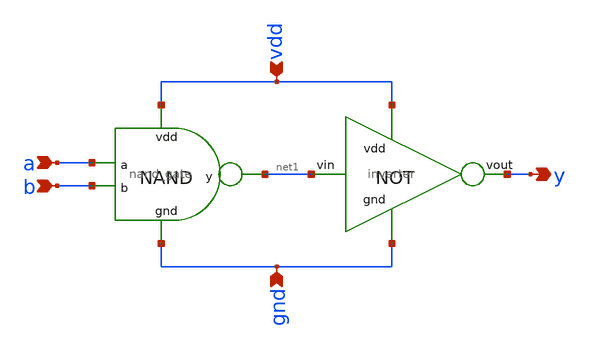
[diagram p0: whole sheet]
** sch_path: sram/and_gate.sch
**.subckt and_gate a b vdd gnd y
*.ipin a
*.ipin b
*.ipin vdd
*.ipin gnd
*.opin y
x2 vdd net1 y gnd inverter
x1 vdd a b gnd net1 nand_gate
**.ends

* expanding   symbol:  inverter.sym # of pins=4
** sym_path: sram/inverter.sym
** sch_path: sram/inverter.sch
.subckt inverter vdd vin vout gnd
*.ipin vin
*.ipin vdd
*.ipin gnd
*.opin vout
XM1 vout vin gnd gnd sky130_fd_pr__nfet_01v8 L=0.15 W=1 nf=1 ad='int((nf+1)/2) * W/nf * 0.29' as='int((nf+2)/2) * W/nf * 0.29'
+ pd='2*int((nf+1)/2) * (W/nf + 0.29)' ps='2*int((nf+2)/2) * (W/nf + 0.29)' nrd='0.29 / W' nrs='0.29 / W'
+ sa=0 sb=0 sd=0 mult=1 m=1
XM2 vout vin vdd vdd sky130_fd_pr__pfet_01v8 L=0.15 W=1 nf=1 ad='int((nf+1)/2) * W/nf * 0.29' as='int((nf+2)/2) * W/nf * 0.29'
+ pd='2*int((nf+1)/2) * (W/nf + 0.29)' ps='2*int((nf+2)/2) * (W/nf + 0.29)' nrd='0.29 / W' nrs='0.29 / W'
+ sa=0 sb=0 sd=0 mult=1 m=1
.ends


* expanding   symbol:  nand_gate.sym # of pins=5
** sym_path: sram/nand_gate.sym
** sch_path: sram/nand_gate.sch
.subckt nand_gate vdd a b gnd y
*.ipin a
*.ipin b
*.ipin vdd
*.ipin gnd
*.opin y
XM1 y a vdd vdd sky130_fd_pr__pfet_01v8 L=0.15 W=1 nf=1 ad='int((nf+1)/2) * W/nf * 0.29' as='int((nf+2)/2) * W/nf * 0.29'
+ pd='2*int((nf+1)/2) * (W/nf + 0.29)' ps='2*int((nf+2)/2) * (W/nf + 0.29)' nrd='0.29 / W' nrs='0.29 / W'
+ sa=0 sb=0 sd=0 mult=1 m=1
XM2 y a net1 net1 sky130_fd_pr__nfet_01v8 L=0.15 W=1 nf=1 ad='int((nf+1)/2) * W/nf * 0.29' as='int((nf+2)/2) * W/nf * 0.29'
+ pd='2*int((nf+1)/2) * (W/nf + 0.29)' ps='2*int((nf+2)/2) * (W/nf + 0.29)' nrd='0.29 / W' nrs='0.29 / W'
+ sa=0 sb=0 sd=0 mult=1 m=1
XM3 y b vdd vdd sky130_fd_pr__pfet_01v8 L=0.15 W=1 nf=1 ad='int((nf+1)/2) * W/nf * 0.29' as='int((nf+2)/2) * W/nf * 0.29'
+ pd='2*int((nf+1)/2) * (W/nf + 0.29)' ps='2*int((nf+2)/2) * (W/nf + 0.29)' nrd='0.29 / W' nrs='0.29 / W'
+ sa=0 sb=0 sd=0 mult=1 m=1
XM4 net1 b gnd gnd sky130_fd_pr__nfet_01v8 L=0.15 W=1 nf=1 ad='int((nf+1)/2) * W/nf * 0.29' as='int((nf+2)/2) * W/nf * 0.29'
+ pd='2*int((nf+1)/2) * (W/nf + 0.29)' ps='2*int((nf+2)/2) * (W/nf + 0.29)' nrd='0.29 / W' nrs='0.29 / W'
+ sa=0 sb=0 sd=0 mult=1 m=1
.ends

.end
